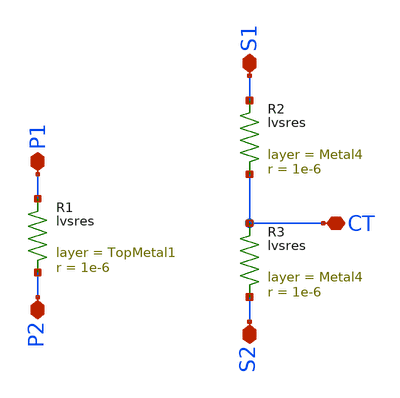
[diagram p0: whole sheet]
** sch_path: ihp-sg13cmos5l/schematic/xschem/sg13_balun_lvsres.sch
**.subckt sg13_balun_lvsres P1 P2 S1 S2 CT
*.iopin P1
*.iopin P2
*.iopin S1
*.iopin S2
*.iopin CT
RR1 P1 P2 1e-6
RR2 S1 CT 1e-6
RR3 CT S2 1e-6
**.ends
.end
